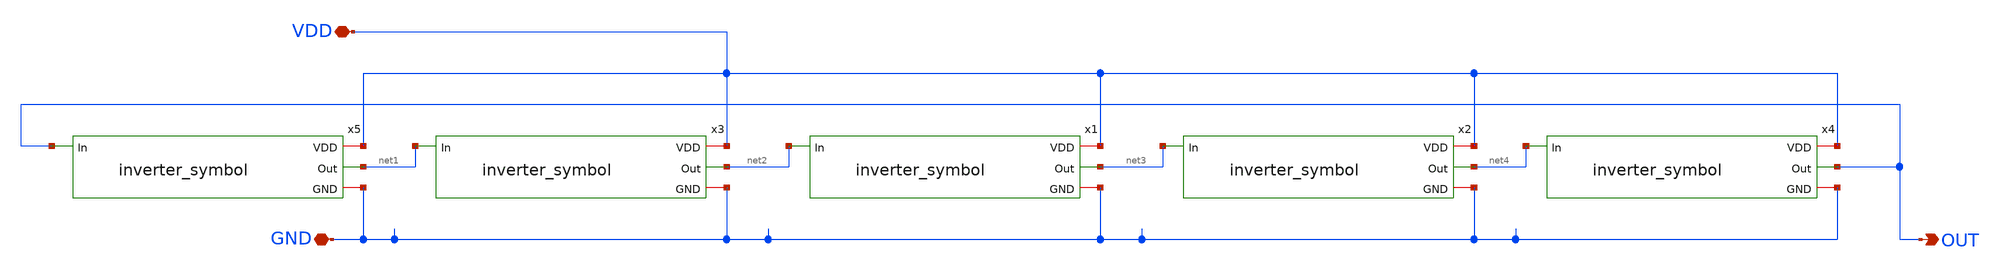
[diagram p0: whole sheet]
** sch_path: schematics/Layouting/ring_oscillator.sch
**.subckt ring_oscillator VDD GND OUT
*.iopin VDD
*.iopin GND
*.opin OUT
x1 VDD net2 net3 GND inverter_symbol
x2 VDD net3 net4 GND inverter_symbol
x3 VDD net1 net2 GND inverter_symbol
x4 VDD net4 OUT GND inverter_symbol
x5 VDD OUT net1 GND inverter_symbol
**.ends

* expanding   symbol:  /home/raditya/Silicons/Projects/inverter_symbol.sym # of pins=4
** sym_path: schematics/Layouting/inverter_symbol.sym
** sch_path: schematics/Layouting/inverter_symbol.sch
.subckt inverter_symbol VDD In Out GND
*.ipin In
*.opin Out
*.iopin VDD
*.iopin GND
XM9 Out In GND GND sky130_fd_pr__nfet_01v8 L=0.15 W=1 nf=1 ad='int((nf+1)/2) * W/nf * 0.29' as='int((nf+2)/2) * W/nf * 0.29'
+ pd='2*int((nf+1)/2) * (W/nf + 0.29)' ps='2*int((nf+2)/2) * (W/nf + 0.29)' nrd='0.29 / W' nrs='0.29 / W'
+ sa=0 sb=0 sd=0 mult=1 m=1
XM10 Out In VDD VDD sky130_fd_pr__pfet_01v8 L=0.15 W=1 nf=1 ad='int((nf+1)/2) * W/nf * 0.29' as='int((nf+2)/2) * W/nf * 0.29'
+ pd='2*int((nf+1)/2) * (W/nf + 0.29)' ps='2*int((nf+2)/2) * (W/nf + 0.29)' nrd='0.29 / W' nrs='0.29 / W'
+ sa=0 sb=0 sd=0 mult=1 m=1
.ends

.end
